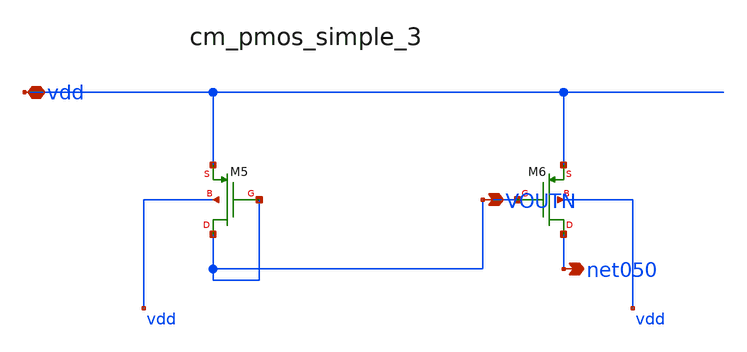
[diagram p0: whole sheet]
** sch_path: analog-db/raw/amp_017_tan_clia/hier/blocks/cm_pmos_simple_3.sch
**.subckt cm_pmos_simple_3 vdd VOUTN net050
*.iopin vdd
*.opin VOUTN
*.opin net050
XM5 VOUTN VOUTN vdd vdd sg13_lv_pmos w=x_dut_xm5_w l=x_dut_xm5_l ng=1 m=x_dut_xm5_m
XM6 net050 VOUTN vdd vdd sg13_lv_pmos w=x_dut_xm6_w l=x_dut_xm6_l ng=1 m=x_dut_xm6_m
**.ends
.end
